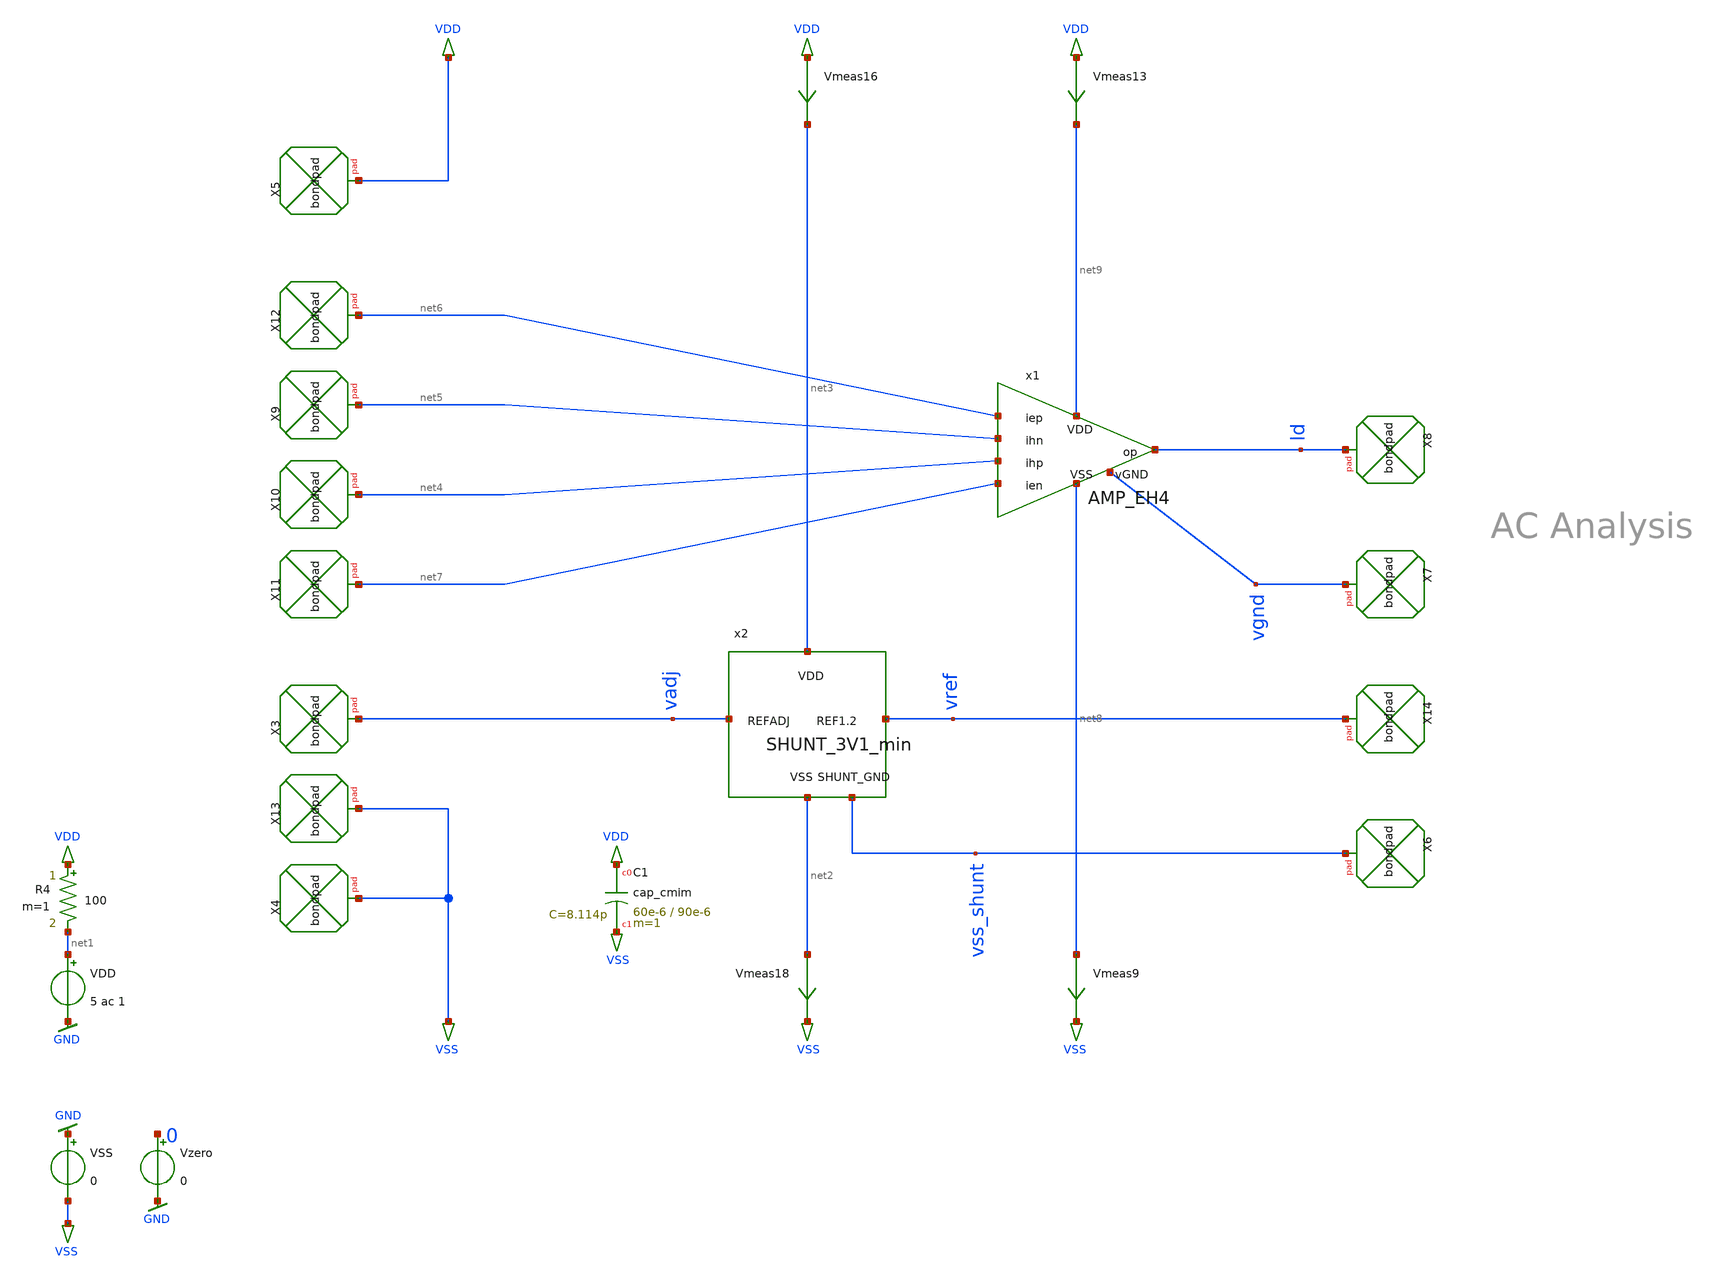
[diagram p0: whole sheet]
** sch_path: HBT_AMP2/design_data/xschem/chip/FMD_QNC_HBT_AMP_EH.02.sch
* Copyright (C) 1998-2023 Stefan Frederik Schippers
* This program is free software; you can redistribute it and/or modify
* it under the terms of the GNU General Public License as published by
* the Free Software Foundation; either version 2 of the License, or
* (at your option) any later version.
* This program is distributed in the hope that it will be useful,
* but WITHOUT ANY WARRANTY; without even the implied warranty of
* MERCHANTABILITY or FITNESS FOR A PARTICULAR PURPOSE.  See the
* GNU General Public License for more details.
* You should have received a copy of the GNU General Public License
* along with this program; if not, write to the Free Software
**.subckt FMD_QNC_HBT_AMP_EH.02
VDD net1 GND 5 ac 1
VSS GND VSS 0
Vzero 0 GND 0
Vmeas13 VDD net9 0
.save i(vmeas13)
Vmeas16 VDD net3 0
.save i(vmeas16)
Vmeas18 net2 VSS 0
.save i(vmeas18)
Vmeas9 net8 VSS 0
.save i(vmeas9)
R4 VDD net1 100 m=1
x2 net3 vref vadj vss_shunt net2 SHUNT_3V1_min
XX3 vadj bondpad size=80u shape=0 padtype=0
XX4 VSS bondpad size=80u shape=0 padtype=0
XX5 VDD bondpad size=80u shape=0 padtype=0
XX6 vss_shunt bondpad size=80u shape=0 padtype=0
XX7 vgnd bondpad size=80u shape=0 padtype=0
XX8 ld bondpad size=80u shape=0 padtype=0
XX9 net5 bondpad size=80u shape=0 padtype=0
XX10 net4 bondpad size=80u shape=0 padtype=0
XX11 net7 bondpad size=80u shape=0 padtype=0
XX12 net6 bondpad size=80u shape=0 padtype=0
XX14 vref bondpad size=80u shape=0 padtype=0
XX13 VSS bondpad size=80u shape=0 padtype=0
XC1 VDD VSS cap_cmim w=60e-6 l=90e-6 m=1 mm_ok=1
x1 net9 vgnd net6 net5 net4 net7 ld net8 AMP_EH4
**** begin user architecture code









**** end user architecture code
**.ends
.GLOBAL GND
.end
